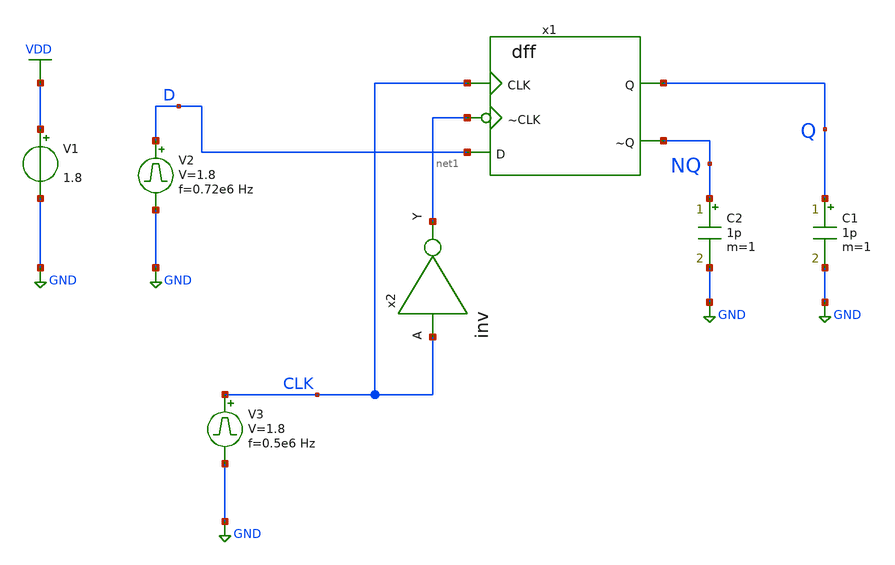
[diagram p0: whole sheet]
** sch_path: xschem/dff_tb.sch
**.subckt dff_tb
V1 VDD GND 1.8
V2 D GND pulse 0 1.8 '0.495/ 0.72e6 ' '0.01/0.72e6 ' '0.01/0.72e6 ' '0.49/0.72e6 ' '1/0.72e6 '
C1 Q GND 1p m=1
V3 CLK GND pulse 0 1.8 '0.495/ 0.5e6 ' '0.01/0.5e6 ' '0.01/0.5e6 ' '0.49/0.5e6 ' '1/0.5e6 '
x2 net1 CLK inv
x1 net1 D NQ Q CLK dff
C2 NQ GND 1p m=1
**** begin user architecture code


.control
save all
tran 1n 10u
plot V(D) V(CLK)+2 V(Q)+4 V(NQ)+6
.endc



** opencircuitdesign pdks install
.lib $::SKYWATER_MODELS/sky130.lib.spice tt


**** end user architecture code
**.ends

* expanding   symbol:  lab1/inv.sym # of pins=2
** sym_path: library/xschem/lab1/inv.sym
** sch_path: library/xschem/lab1/inv.sch
.subckt inv Y A
*.ipin A
*.opin Y
XM1 Y A GND GND sky130_fd_pr__nfet_01v8 L=0.15 W=0.5 nf=1 ad='int((nf+1)/2) * W/nf * 0.29' as='int((nf+2)/2) * W/nf * 0.29'
+ pd='2*int((nf+1)/2) * (W/nf + 0.29)' ps='2*int((nf+2)/2) * (W/nf + 0.29)' nrd='0.29 / W' nrs='0.29 / W'
+ sa=0 sb=0 sd=0 mult=1 m=1
XM2 Y A VDD VDD sky130_fd_pr__pfet_01v8 L=0.15 W=1 nf=1 ad='int((nf+1)/2) * W/nf * 0.29' as='int((nf+2)/2) * W/nf * 0.29'
+ pd='2*int((nf+1)/2) * (W/nf + 0.29)' ps='2*int((nf+2)/2) * (W/nf + 0.29)' nrd='0.29 / W' nrs='0.29 / W'
+ sa=0 sb=0 sd=0 mult=1 m=1
.ends


* expanding   symbol:  dff.sym # of pins=5
** sym_path: xschem/dff.sym
** sch_path: xschem/dff.sch
.subckt dff ~CLK D ~Q Q CLK
*.ipin D
*.ipin ~CLK
*.ipin CLK
*.opin ~Q
*.opin Q
XM5 net1 ~CLK net2 VDD sky130_fd_pr__pfet_01v8 L=0.15 W=1 nf=1 ad='int((nf+1)/2) * W/nf * 0.29' as='int((nf+2)/2) * W/nf * 0.29'
+ pd='2*int((nf+1)/2) * (W/nf + 0.29)' ps='2*int((nf+2)/2) * (W/nf + 0.29)' nrd='0.29 / W' nrs='0.29 / W'
+ sa=0 sb=0 sd=0 mult=1 m=1
XM6 net1 CLK net2 GND sky130_fd_pr__nfet_01v8 L=0.15 W=0.5 nf=1 ad='int((nf+1)/2) * W/nf * 0.29' as='int((nf+2)/2) * W/nf * 0.29'
+ pd='2*int((nf+1)/2) * (W/nf + 0.29)' ps='2*int((nf+2)/2) * (W/nf + 0.29)' nrd='0.29 / W' nrs='0.29 / W'
+ sa=0 sb=0 sd=0 mult=1 m=1
XM7 D CLK net1 VDD sky130_fd_pr__pfet_01v8 L=0.15 W=1 nf=1 ad='int((nf+1)/2) * W/nf * 0.29' as='int((nf+2)/2) * W/nf * 0.29'
+ pd='2*int((nf+1)/2) * (W/nf + 0.29)' ps='2*int((nf+2)/2) * (W/nf + 0.29)' nrd='0.29 / W' nrs='0.29 / W'
+ sa=0 sb=0 sd=0 mult=1 m=1
XM8 D ~CLK net1 GND sky130_fd_pr__nfet_01v8 L=0.15 W=0.5 nf=1 ad='int((nf+1)/2) * W/nf * 0.29' as='int((nf+2)/2) * W/nf * 0.29'
+ pd='2*int((nf+1)/2) * (W/nf + 0.29)' ps='2*int((nf+2)/2) * (W/nf + 0.29)' nrd='0.29 / W' nrs='0.29 / W'
+ sa=0 sb=0 sd=0 mult=1 m=1
XM9 net3 net1 VDD VDD sky130_fd_pr__pfet_01v8 L=0.15 W=1 nf=1 ad='int((nf+1)/2) * W/nf * 0.29' as='int((nf+2)/2) * W/nf * 0.29'
+ pd='2*int((nf+1)/2) * (W/nf + 0.29)' ps='2*int((nf+2)/2) * (W/nf + 0.29)' nrd='0.29 / W' nrs='0.29 / W'
+ sa=0 sb=0 sd=0 mult=1 m=1
XM10 net3 net1 GND GND sky130_fd_pr__nfet_01v8 L=0.15 W=0.5 nf=1 ad='int((nf+1)/2) * W/nf * 0.29' as='int((nf+2)/2) * W/nf * 0.29'
+ pd='2*int((nf+1)/2) * (W/nf + 0.29)' ps='2*int((nf+2)/2) * (W/nf + 0.29)' nrd='0.29 / W' nrs='0.29 / W'
+ sa=0 sb=0 sd=0 mult=1 m=1
XM11 net2 net3 VDD VDD sky130_fd_pr__pfet_01v8 L=0.15 W=1 nf=1 ad='int((nf+1)/2) * W/nf * 0.29' as='int((nf+2)/2) * W/nf * 0.29'
+ pd='2*int((nf+1)/2) * (W/nf + 0.29)' ps='2*int((nf+2)/2) * (W/nf + 0.29)' nrd='0.29 / W' nrs='0.29 / W'
+ sa=0 sb=0 sd=0 mult=1 m=1
XM12 net2 net3 GND GND sky130_fd_pr__nfet_01v8 L=0.15 W=0.5 nf=1 ad='int((nf+1)/2) * W/nf * 0.29' as='int((nf+2)/2) * W/nf * 0.29'
+ pd='2*int((nf+1)/2) * (W/nf + 0.29)' ps='2*int((nf+2)/2) * (W/nf + 0.29)' nrd='0.29 / W' nrs='0.29 / W'
+ sa=0 sb=0 sd=0 mult=1 m=1
XM1 net4 CLK ~Q VDD sky130_fd_pr__pfet_01v8 L=0.15 W=1 nf=1 ad='int((nf+1)/2) * W/nf * 0.29' as='int((nf+2)/2) * W/nf * 0.29'
+ pd='2*int((nf+1)/2) * (W/nf + 0.29)' ps='2*int((nf+2)/2) * (W/nf + 0.29)' nrd='0.29 / W' nrs='0.29 / W'
+ sa=0 sb=0 sd=0 mult=1 m=1
XM2 net4 ~CLK ~Q GND sky130_fd_pr__nfet_01v8 L=0.15 W=0.5 nf=1 ad='int((nf+1)/2) * W/nf * 0.29' as='int((nf+2)/2) * W/nf * 0.29'
+ pd='2*int((nf+1)/2) * (W/nf + 0.29)' ps='2*int((nf+2)/2) * (W/nf + 0.29)' nrd='0.29 / W' nrs='0.29 / W'
+ sa=0 sb=0 sd=0 mult=1 m=1
XM3 Q net4 VDD VDD sky130_fd_pr__pfet_01v8 L=0.15 W=1 nf=1 ad='int((nf+1)/2) * W/nf * 0.29' as='int((nf+2)/2) * W/nf * 0.29'
+ pd='2*int((nf+1)/2) * (W/nf + 0.29)' ps='2*int((nf+2)/2) * (W/nf + 0.29)' nrd='0.29 / W' nrs='0.29 / W'
+ sa=0 sb=0 sd=0 mult=1 m=1
XM4 Q net4 GND GND sky130_fd_pr__nfet_01v8 L=0.15 W=0.5 nf=1 ad='int((nf+1)/2) * W/nf * 0.29' as='int((nf+2)/2) * W/nf * 0.29'
+ pd='2*int((nf+1)/2) * (W/nf + 0.29)' ps='2*int((nf+2)/2) * (W/nf + 0.29)' nrd='0.29 / W' nrs='0.29 / W'
+ sa=0 sb=0 sd=0 mult=1 m=1
XM13 ~Q Q VDD VDD sky130_fd_pr__pfet_01v8 L=0.15 W=1 nf=1 ad='int((nf+1)/2) * W/nf * 0.29' as='int((nf+2)/2) * W/nf * 0.29'
+ pd='2*int((nf+1)/2) * (W/nf + 0.29)' ps='2*int((nf+2)/2) * (W/nf + 0.29)' nrd='0.29 / W' nrs='0.29 / W'
+ sa=0 sb=0 sd=0 mult=1 m=1
XM14 ~Q Q GND GND sky130_fd_pr__nfet_01v8 L=0.15 W=0.5 nf=1 ad='int((nf+1)/2) * W/nf * 0.29' as='int((nf+2)/2) * W/nf * 0.29'
+ pd='2*int((nf+1)/2) * (W/nf + 0.29)' ps='2*int((nf+2)/2) * (W/nf + 0.29)' nrd='0.29 / W' nrs='0.29 / W'
+ sa=0 sb=0 sd=0 mult=1 m=1
XM15 net3 ~CLK net4 VDD sky130_fd_pr__pfet_01v8 L=0.15 W=1 nf=1 ad='int((nf+1)/2) * W/nf * 0.29' as='int((nf+2)/2) * W/nf * 0.29'
+ pd='2*int((nf+1)/2) * (W/nf + 0.29)' ps='2*int((nf+2)/2) * (W/nf + 0.29)' nrd='0.29 / W' nrs='0.29 / W'
+ sa=0 sb=0 sd=0 mult=1 m=1
XM16 net3 CLK net4 GND sky130_fd_pr__nfet_01v8 L=0.15 W=0.5 nf=1 ad='int((nf+1)/2) * W/nf * 0.29' as='int((nf+2)/2) * W/nf * 0.29'
+ pd='2*int((nf+1)/2) * (W/nf + 0.29)' ps='2*int((nf+2)/2) * (W/nf + 0.29)' nrd='0.29 / W' nrs='0.29 / W'
+ sa=0 sb=0 sd=0 mult=1 m=1
.ends

.GLOBAL VDD
.GLOBAL GND
.end
